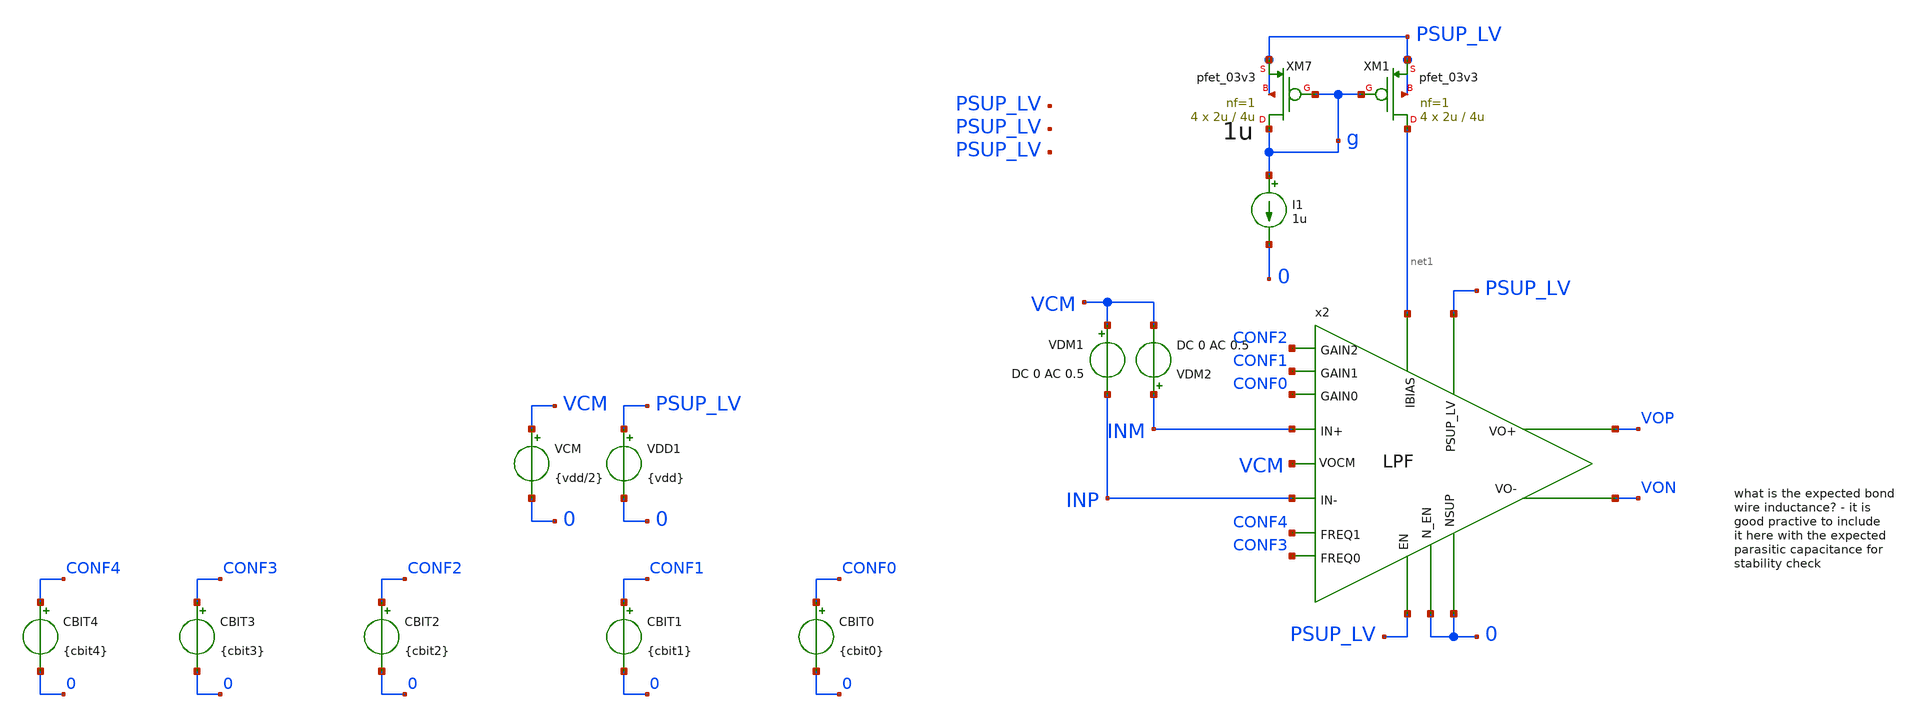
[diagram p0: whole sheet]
** sch_path: xschem/blocks/LPF/tb_LPF_gain.sch
**.subckt tb_LPF_gain
VDD1 PSUP_LV 0 {vdd}
VCM VCM 0 {vdd/2}
VDM2 INM VCM DC 0 AC 0.5
VDM1 VCM INP DC 0 AC 0.5
x2 PSUP_LV 0 PSUP_LV 0 net1 CONF2 CONF1 CONF0 CONF4 CONF3 INM VOP VCM INP VON LPF
XM7 g g PSUP_LV PSUP_LV pfet_03v3 L=4u W=2u nf=1 ad='int((nf+1)/2) * W/nf * 0.18u' as='int((nf+2)/2) * W/nf * 0.18u'
+ pd='2*int((nf+1)/2) * (W/nf + 0.18u)' ps='2*int((nf+2)/2) * (W/nf + 0.18u)' nrd='0.18u / W' nrs='0.18u / W'
+ sa=0 sb=0 sd=0 m=4
XM1 net1 g PSUP_LV PSUP_LV pfet_03v3 L=4u W=2u nf=1 ad='int((nf+1)/2) * W/nf * 0.18u' as='int((nf+2)/2) * W/nf * 0.18u'
+ pd='2*int((nf+1)/2) * (W/nf + 0.18u)' ps='2*int((nf+2)/2) * (W/nf + 0.18u)' nrd='0.18u / W' nrs='0.18u / W'
+ sa=0 sb=0 sd=0 m=4
I1 g 0 1u
CBIT2 CONF2 0 {cbit2}
CBIT1 CONF1 0 {cbit1}
CBIT0 CONF0 0 {cbit0}
CBIT4 CONF4 0 {cbit4}
CBIT3 CONF3 0 {cbit3}
**** begin user architecture code

.include $::180MCU_MODELS/design.ngspice

.lib $::180MCU_MODELS/sm141064.ngspice typical
.lib $::180MCU_MODELS/sm141064.ngspice res_typical
.lib $::180MCU_MODELS/sm141064.ngspice bjt_typical
.lib $::180MCU_MODELS/sm141064.ngspice mimcap_typical
.lib $::180MCU_MODELS/sm141064.ngspice cap_mim

.temp 25

.param vdd=3.3

.param cbit0=1
.param cbit1=0
.param cbit2=1
.param cbit3=0
.param cbit4=0

* Deterministic PVT: disable random global/mismatch variation.
.param sw_stat_global=0
.param sw_stat_mismatch=0



.control
set units=degrees
save all
ac dec 100 1 1G

let Vid = v(INP) - v(INM)
let Vo = v(Vop) - v(Von)
let aol = v(Vo) / v(Vid)
let gain_db = db(aol)
let phase_deg = cph(aol)

*write tb_LPF_gain.raw gain_db phase_deg
write tb_LPF_gain.raw

.endc


**** end user architecture code
**.ends
.end
